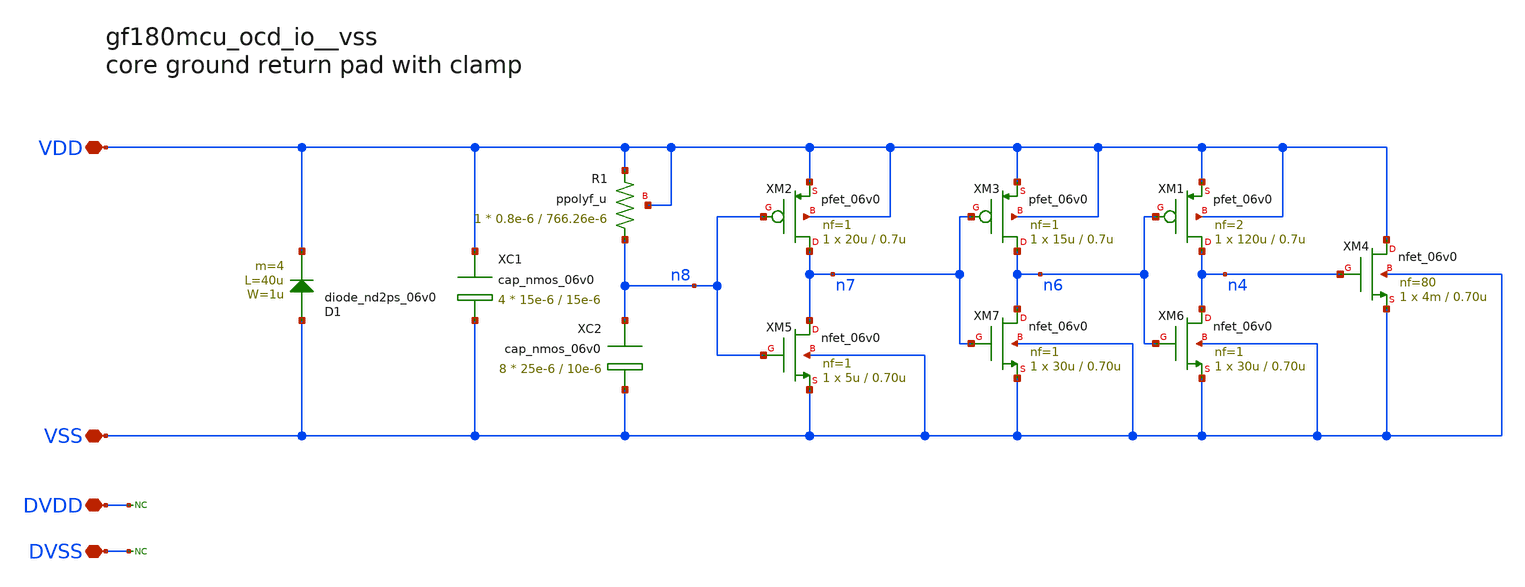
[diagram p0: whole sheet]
** sch_path: cells/vss/gf180mcu_ocd_io__vss.sch
**.subckt gf180mcu_ocd_io__vss DVDD DVSS VDD VSS
*.iopin DVDD
*.iopin DVSS
*.iopin VDD
*.iopin VSS
D1 VSS VDD diode_nd2ps_06v0 area='1u * 40u ' pj='2*1u + 2*40u ' m=4
XC1 VDD VSS cap_nmos_06v0 c_width=15e-6 c_length=15e-6 m=4
* noconn DVDD
XM1 n4 n6 VDD VDD pfet_06v0 L=0.7u W=120u nf=2 ad='int((nf+1)/2) * W/nf * 0.18u' as='int((nf+2)/2) * W/nf * 0.18u'
+ pd='2*int((nf+1)/2) * (W/nf + 0.18u)' ps='2*int((nf+2)/2) * (W/nf + 0.18u)' nrd='0.18u / W' nrs='0.18u / W'
+ sa=0 sb=0 sd=0 m=1
XM2 n7 n8 VDD VDD pfet_06v0 L=0.7u W=20u nf=1 ad='int((nf+1)/2) * W/nf * 0.18u' as='int((nf+2)/2) * W/nf * 0.18u'
+ pd='2*int((nf+1)/2) * (W/nf + 0.18u)' ps='2*int((nf+2)/2) * (W/nf + 0.18u)' nrd='0.18u / W' nrs='0.18u / W'
+ sa=0 sb=0 sd=0 m=1
XM3 n6 n7 VDD VDD pfet_06v0 L=0.7u W=15u nf=1 ad='int((nf+1)/2) * W/nf * 0.18u' as='int((nf+2)/2) * W/nf * 0.18u'
+ pd='2*int((nf+1)/2) * (W/nf + 0.18u)' ps='2*int((nf+2)/2) * (W/nf + 0.18u)' nrd='0.18u / W' nrs='0.18u / W'
+ sa=0 sb=0 sd=0 m=1
XC2 n8 VSS cap_nmos_06v0 c_width=25e-6 c_length=10e-6 m=8
XM4 VDD n4 VSS VSS nfet_06v0 L=0.70u W=4m nf=80 ad='int((nf+1)/2) * W/nf * 0.18u' as='int((nf+2)/2) * W/nf * 0.18u'
+ pd='2*int((nf+1)/2) * (W/nf + 0.18u)' ps='2*int((nf+2)/2) * (W/nf + 0.18u)' nrd='0.18u / W' nrs='0.18u / W'
+ sa=0 sb=0 sd=0 m=1
XM5 n7 n8 VSS VSS nfet_06v0 L=0.70u W=5u nf=1 ad='int((nf+1)/2) * W/nf * 0.18u' as='int((nf+2)/2) * W/nf * 0.18u'
+ pd='2*int((nf+1)/2) * (W/nf + 0.18u)' ps='2*int((nf+2)/2) * (W/nf + 0.18u)' nrd='0.18u / W' nrs='0.18u / W'
+ sa=0 sb=0 sd=0 m=1
XM6 n4 n6 VSS VSS nfet_06v0 L=0.70u W=30u nf=1 ad='int((nf+1)/2) * W/nf * 0.18u' as='int((nf+2)/2) * W/nf * 0.18u'
+ pd='2*int((nf+1)/2) * (W/nf + 0.18u)' ps='2*int((nf+2)/2) * (W/nf + 0.18u)' nrd='0.18u / W' nrs='0.18u / W'
+ sa=0 sb=0 sd=0 m=1
XM7 n6 n7 VSS VSS nfet_06v0 L=0.70u W=30u nf=1 ad='int((nf+1)/2) * W/nf * 0.18u' as='int((nf+2)/2) * W/nf * 0.18u'
+ pd='2*int((nf+1)/2) * (W/nf + 0.18u)' ps='2*int((nf+2)/2) * (W/nf + 0.18u)' nrd='0.18u / W' nrs='0.18u / W'
+ sa=0 sb=0 sd=0 m=1
XR1 n8 VDD VDD ppolyf_u r_width=0.8e-6 r_length=766.26e-6 m=1
* noconn DVSS
**.ends
.end
